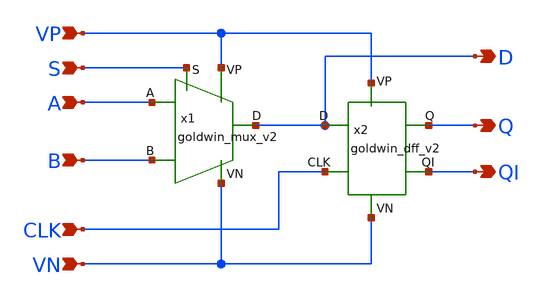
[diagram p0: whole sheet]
** sch_path: APIC-UTS/schematic/goldwin_mux_dff_v2/goldwin_mux_dff_v2.sch
**.subckt goldwin_mux_dff_v2 A B S CLK VP VN Q QI D
*.ipin A
*.ipin B
*.ipin S
*.ipin CLK
*.ipin VP
*.ipin VN
*.opin Q
*.opin QI
*.opin D
x1 A B S D VP VN goldwin_mux_v2
x2 D CLK VP VN Q QI VP VN goldwin_dff_v2
**.ends
.end
